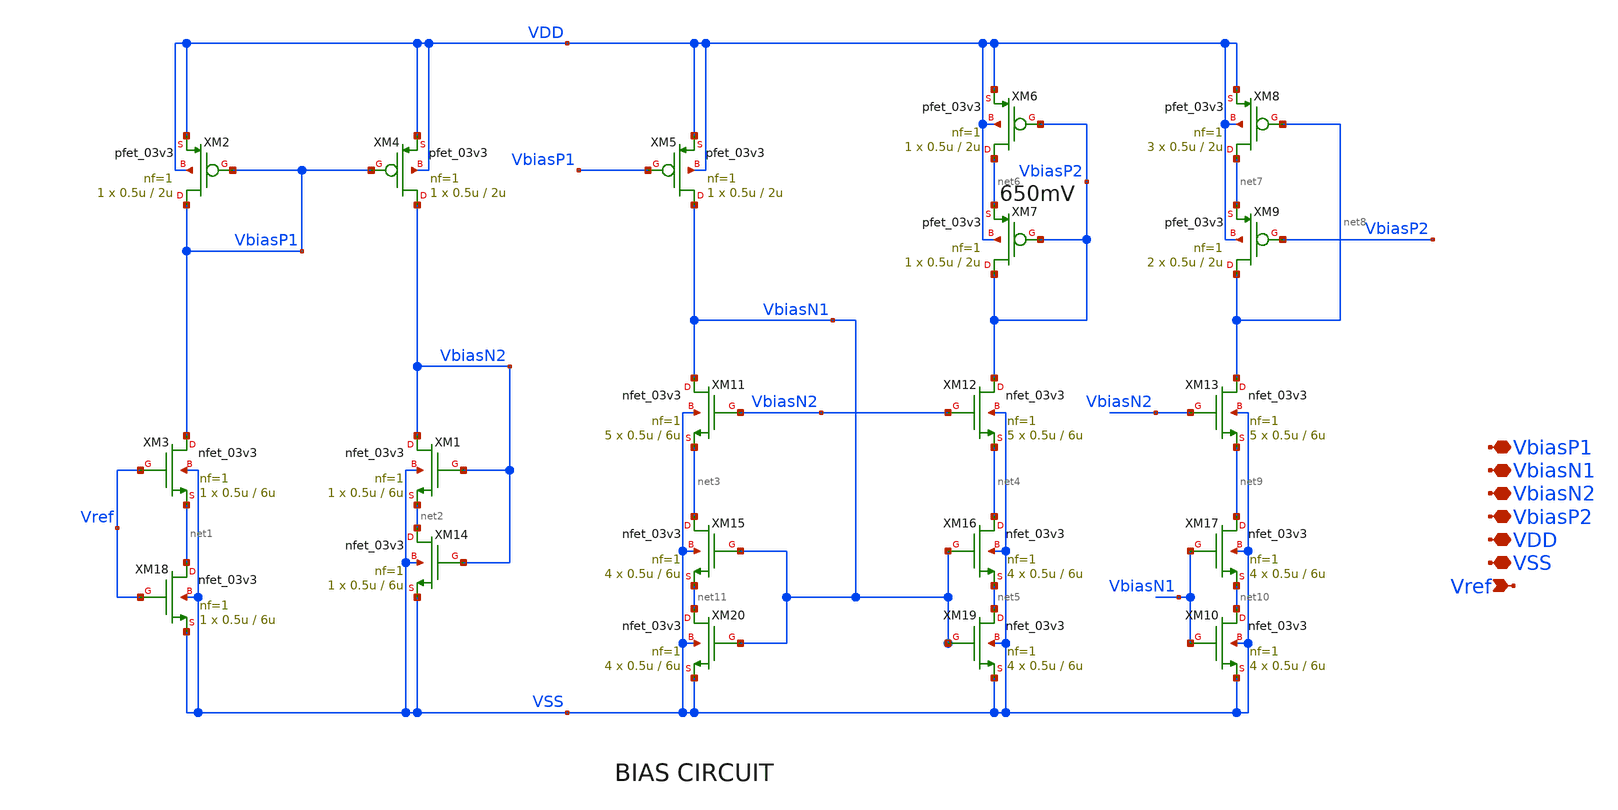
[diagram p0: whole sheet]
** sch_path: blocks/composite/folded_cascode/designs/gf180/error_amplifier_bias_N_input/xschem/error_amplifier_bias_N_input.sch
**.subckt error_amplifier_bias_N_input Vref VbiasN1 VbiasN2 VDD VbiasP2 VSS VbiasP1
*.ipin Vref
*.iopin VbiasN1
*.iopin VbiasN2
*.iopin VDD
*.iopin VbiasP2
*.iopin VSS
*.iopin VbiasP1
XM1 VbiasN2 VbiasN2 net2 VSS nfet_03v3 L=6u W=0.5u nf=1 ad='int((nf+1)/2) * W/nf * 0.18u' as='int((nf+2)/2) * W/nf * 0.18u'
+ pd='2*int((nf+1)/2) * (W/nf + 0.18u)' ps='2*int((nf+2)/2) * (W/nf + 0.18u)' nrd='0.18u / W' nrs='0.18u / W'
+ sa=0 sb=0 sd=0 m=1
XM2 VbiasP1 VbiasP1 VDD VDD pfet_03v3 L=2u W=0.5u nf=1 ad='int((nf+1)/2) * W/nf * 0.18u' as='int((nf+2)/2) * W/nf * 0.18u'
+ pd='2*int((nf+1)/2) * (W/nf + 0.18u)' ps='2*int((nf+2)/2) * (W/nf + 0.18u)' nrd='0.18u / W' nrs='0.18u / W'
+ sa=0 sb=0 sd=0 m=1
XM3 VbiasP1 Vref net1 VSS nfet_03v3 L=6u W=0.5u nf=1 ad='int((nf+1)/2) * W/nf * 0.18u' as='int((nf+2)/2) * W/nf * 0.18u'
+ pd='2*int((nf+1)/2) * (W/nf + 0.18u)' ps='2*int((nf+2)/2) * (W/nf + 0.18u)' nrd='0.18u / W' nrs='0.18u / W'
+ sa=0 sb=0 sd=0 m=1
XM4 VbiasN2 VbiasP1 VDD VDD pfet_03v3 L=2u W=0.5u nf=1 ad='int((nf+1)/2) * W/nf * 0.18u' as='int((nf+2)/2) * W/nf * 0.18u'
+ pd='2*int((nf+1)/2) * (W/nf + 0.18u)' ps='2*int((nf+2)/2) * (W/nf + 0.18u)' nrd='0.18u / W' nrs='0.18u / W'
+ sa=0 sb=0 sd=0 m=1
XM5 VbiasN1 VbiasP1 VDD VDD pfet_03v3 L=2u W=0.5u nf=1 ad='int((nf+1)/2) * W/nf * 0.18u' as='int((nf+2)/2) * W/nf * 0.18u'
+ pd='2*int((nf+1)/2) * (W/nf + 0.18u)' ps='2*int((nf+2)/2) * (W/nf + 0.18u)' nrd='0.18u / W' nrs='0.18u / W'
+ sa=0 sb=0 sd=0 m=1
XM6 net6 VbiasP2 VDD VDD pfet_03v3 L=2u W=0.5u nf=1 ad='int((nf+1)/2) * W/nf * 0.18u' as='int((nf+2)/2) * W/nf * 0.18u'
+ pd='2*int((nf+1)/2) * (W/nf + 0.18u)' ps='2*int((nf+2)/2) * (W/nf + 0.18u)' nrd='0.18u / W' nrs='0.18u / W'
+ sa=0 sb=0 sd=0 m=1
XM7 VbiasP2 VbiasP2 net6 VDD pfet_03v3 L=2u W=0.5u nf=1 ad='int((nf+1)/2) * W/nf * 0.18u' as='int((nf+2)/2) * W/nf * 0.18u'
+ pd='2*int((nf+1)/2) * (W/nf + 0.18u)' ps='2*int((nf+2)/2) * (W/nf + 0.18u)' nrd='0.18u / W' nrs='0.18u / W'
+ sa=0 sb=0 sd=0 m=1
XM8 net7 net8 VDD VDD pfet_03v3 L=2u W=0.5u nf=1 ad='int((nf+1)/2) * W/nf * 0.18u' as='int((nf+2)/2) * W/nf * 0.18u'
+ pd='2*int((nf+1)/2) * (W/nf + 0.18u)' ps='2*int((nf+2)/2) * (W/nf + 0.18u)' nrd='0.18u / W' nrs='0.18u / W'
+ sa=0 sb=0 sd=0 m=3
XM9 net8 VbiasP2 net7 VDD pfet_03v3 L=2u W=0.5u nf=1 ad='int((nf+1)/2) * W/nf * 0.18u' as='int((nf+2)/2) * W/nf * 0.18u'
+ pd='2*int((nf+1)/2) * (W/nf + 0.18u)' ps='2*int((nf+2)/2) * (W/nf + 0.18u)' nrd='0.18u / W' nrs='0.18u / W'
+ sa=0 sb=0 sd=0 m=2
XM10 net10 VbiasN1 VSS VSS nfet_03v3 L=6u W=0.5u nf=1 ad='int((nf+1)/2) * W/nf * 0.18u' as='int((nf+2)/2) * W/nf * 0.18u'
+ pd='2*int((nf+1)/2) * (W/nf + 0.18u)' ps='2*int((nf+2)/2) * (W/nf + 0.18u)' nrd='0.18u / W' nrs='0.18u / W'
+ sa=0 sb=0 sd=0 m=4
XM11 VbiasN1 VbiasN2 net3 VSS nfet_03v3 L=6u W=0.5u nf=1 ad='int((nf+1)/2) * W/nf * 0.18u' as='int((nf+2)/2) * W/nf * 0.18u'
+ pd='2*int((nf+1)/2) * (W/nf + 0.18u)' ps='2*int((nf+2)/2) * (W/nf + 0.18u)' nrd='0.18u / W' nrs='0.18u / W'
+ sa=0 sb=0 sd=0 m=5
XM12 VbiasP2 VbiasN2 net4 VSS nfet_03v3 L=6u W=0.5u nf=1 ad='int((nf+1)/2) * W/nf * 0.18u' as='int((nf+2)/2) * W/nf * 0.18u'
+ pd='2*int((nf+1)/2) * (W/nf + 0.18u)' ps='2*int((nf+2)/2) * (W/nf + 0.18u)' nrd='0.18u / W' nrs='0.18u / W'
+ sa=0 sb=0 sd=0 m=5
XM13 net8 VbiasN2 net9 VSS nfet_03v3 L=6u W=0.5u nf=1 ad='int((nf+1)/2) * W/nf * 0.18u' as='int((nf+2)/2) * W/nf * 0.18u'
+ pd='2*int((nf+1)/2) * (W/nf + 0.18u)' ps='2*int((nf+2)/2) * (W/nf + 0.18u)' nrd='0.18u / W' nrs='0.18u / W'
+ sa=0 sb=0 sd=0 m=5
XM14 net2 VbiasN2 VSS VSS nfet_03v3 L=6u W=0.5u nf=1 ad='int((nf+1)/2) * W/nf * 0.18u' as='int((nf+2)/2) * W/nf * 0.18u'
+ pd='2*int((nf+1)/2) * (W/nf + 0.18u)' ps='2*int((nf+2)/2) * (W/nf + 0.18u)' nrd='0.18u / W' nrs='0.18u / W'
+ sa=0 sb=0 sd=0 m=1
XM15 net3 VbiasN1 net11 VSS nfet_03v3 L=6u W=0.5u nf=1 ad='int((nf+1)/2) * W/nf * 0.18u' as='int((nf+2)/2) * W/nf * 0.18u'
+ pd='2*int((nf+1)/2) * (W/nf + 0.18u)' ps='2*int((nf+2)/2) * (W/nf + 0.18u)' nrd='0.18u / W' nrs='0.18u / W'
+ sa=0 sb=0 sd=0 m=4
XM16 net4 VbiasN1 net5 VSS nfet_03v3 L=6u W=0.5u nf=1 ad='int((nf+1)/2) * W/nf * 0.18u' as='int((nf+2)/2) * W/nf * 0.18u'
+ pd='2*int((nf+1)/2) * (W/nf + 0.18u)' ps='2*int((nf+2)/2) * (W/nf + 0.18u)' nrd='0.18u / W' nrs='0.18u / W'
+ sa=0 sb=0 sd=0 m=4
XM17 net9 VbiasN1 net10 VSS nfet_03v3 L=6u W=0.5u nf=1 ad='int((nf+1)/2) * W/nf * 0.18u' as='int((nf+2)/2) * W/nf * 0.18u'
+ pd='2*int((nf+1)/2) * (W/nf + 0.18u)' ps='2*int((nf+2)/2) * (W/nf + 0.18u)' nrd='0.18u / W' nrs='0.18u / W'
+ sa=0 sb=0 sd=0 m=4
XM18 net1 Vref VSS VSS nfet_03v3 L=6u W=0.5u nf=1 ad='int((nf+1)/2) * W/nf * 0.18u' as='int((nf+2)/2) * W/nf * 0.18u'
+ pd='2*int((nf+1)/2) * (W/nf + 0.18u)' ps='2*int((nf+2)/2) * (W/nf + 0.18u)' nrd='0.18u / W' nrs='0.18u / W'
+ sa=0 sb=0 sd=0 m=1
XM19 net5 VbiasN1 VSS VSS nfet_03v3 L=6u W=0.5u nf=1 ad='int((nf+1)/2) * W/nf * 0.18u' as='int((nf+2)/2) * W/nf * 0.18u'
+ pd='2*int((nf+1)/2) * (W/nf + 0.18u)' ps='2*int((nf+2)/2) * (W/nf + 0.18u)' nrd='0.18u / W' nrs='0.18u / W'
+ sa=0 sb=0 sd=0 m=4
XM20 net11 VbiasN1 VSS VSS nfet_03v3 L=6u W=0.5u nf=1 ad='int((nf+1)/2) * W/nf * 0.18u' as='int((nf+2)/2) * W/nf * 0.18u'
+ pd='2*int((nf+1)/2) * (W/nf + 0.18u)' ps='2*int((nf+2)/2) * (W/nf + 0.18u)' nrd='0.18u / W' nrs='0.18u / W'
+ sa=0 sb=0 sd=0 m=4
**.ends
.end
